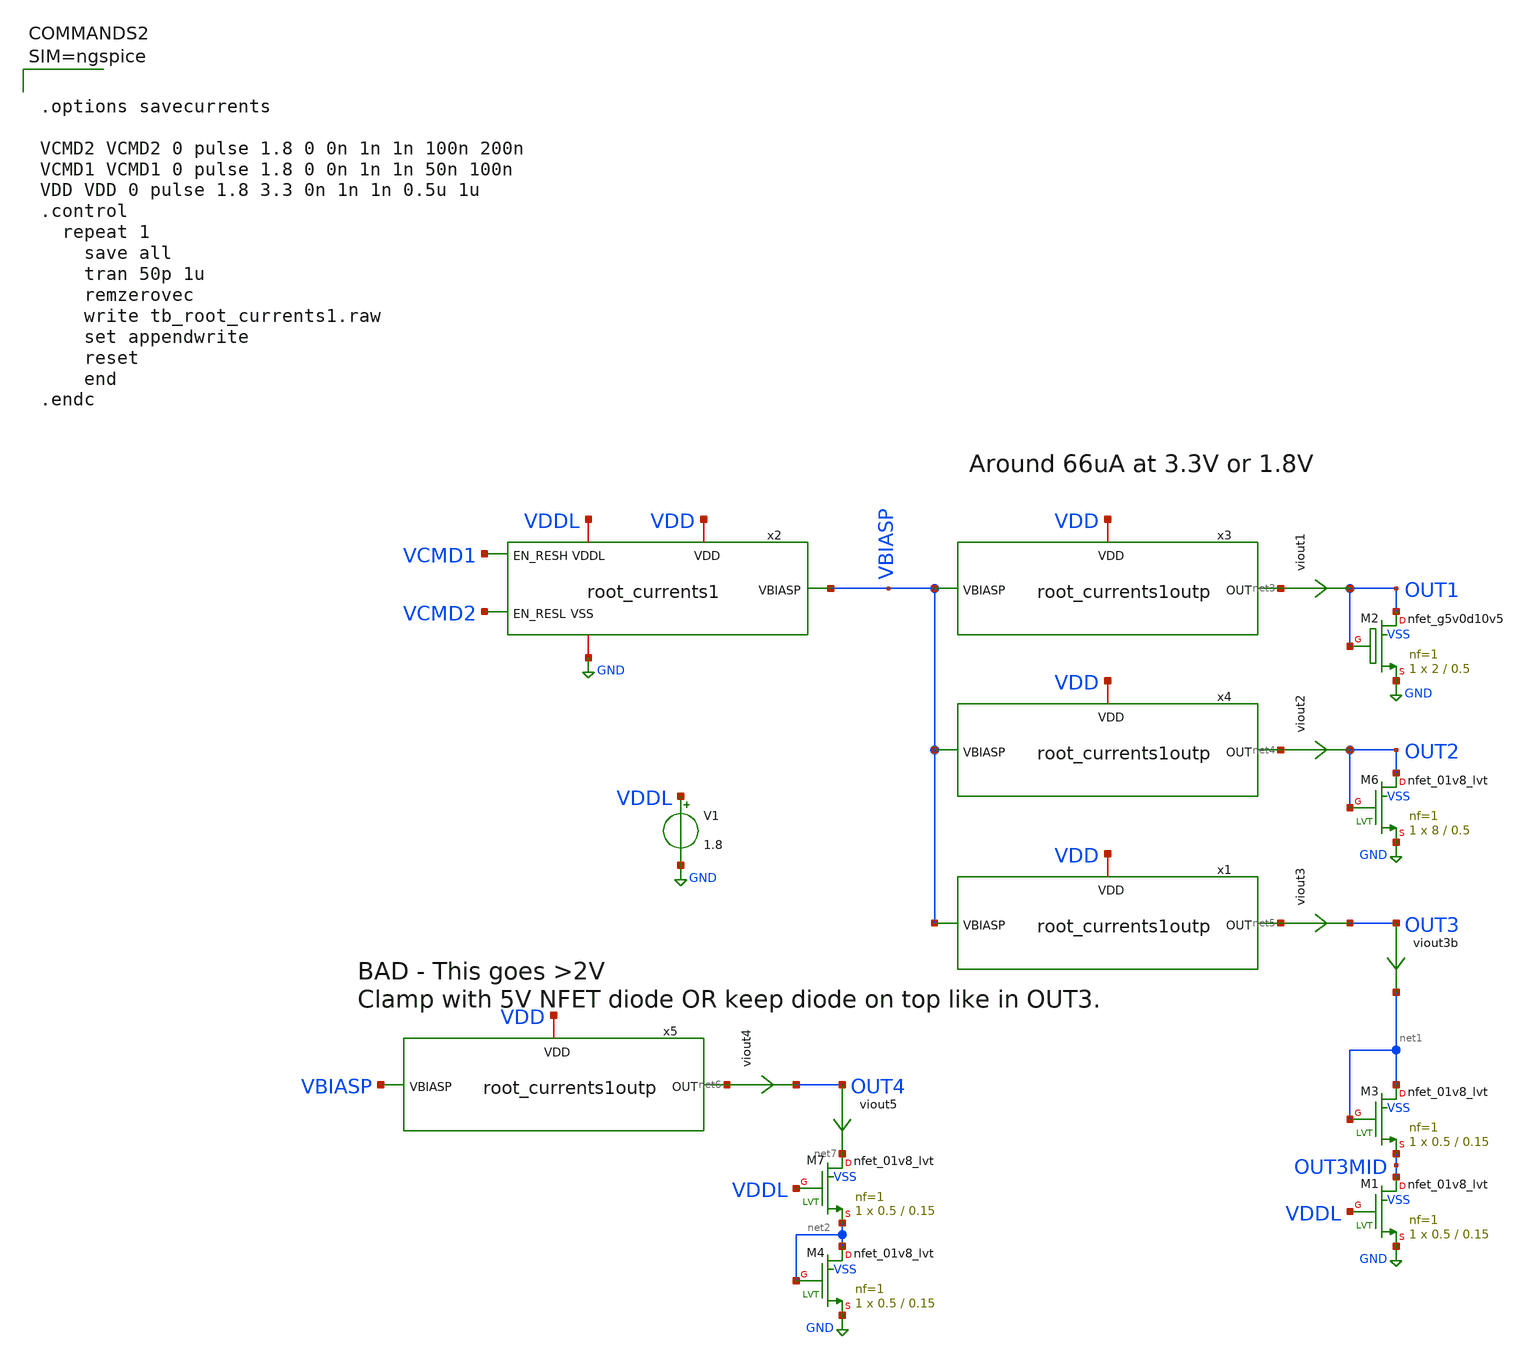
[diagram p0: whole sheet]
** sch_path: xschem/tb_root_currents1.sch
**.subckt tb_root_currents1
x2 VCMD1 VCMD2 VBIASP VDD VDDL GND root_currents1
x3 VBIASP net3 VDD root_currents1outp
x4 VBIASP net4 VDD root_currents1outp
XM6 OUT2 OUT2 GND VSS sky130_fd_pr__nfet_01v8_lvt L=0.5 W=8 nf=1 ad='int((nf+1)/2) * W/nf * 0.29' as='int((nf+2)/2) * W/nf * 0.29'
+ pd='2*int((nf+1)/2) * (W/nf + 0.29)' ps='2*int((nf+2)/2) * (W/nf + 0.29)' nrd='0.29 / W' nrs='0.29 / W'
+ sa=0 sb=0 sd=0 mult=1 m=1
viout1 net3 OUT1 0
.save i(viout1)
viout2 net4 OUT2 0
.save i(viout2)
XM2 OUT1 OUT1 GND VSS sky130_fd_pr__nfet_g5v0d10v5 L=0.5 W=2 nf=1 ad='int((nf+1)/2) * W/nf * 0.29' as='int((nf+2)/2) * W/nf * 0.29'
+ pd='2*int((nf+1)/2) * (W/nf + 0.29)' ps='2*int((nf+2)/2) * (W/nf + 0.29)' nrd='0.29 / W' nrs='0.29 / W'
+ sa=0 sb=0 sd=0 mult=1 m=1
V1 VDDL GND 1.8
x1 VBIASP net5 VDD root_currents1outp
XM1 OUT3MID VDDL GND VSS sky130_fd_pr__nfet_01v8_lvt L=0.15 W=0.5 nf=1 ad='int((nf+1)/2) * W/nf * 0.29'
+ as='int((nf+2)/2) * W/nf * 0.29' pd='2*int((nf+1)/2) * (W/nf + 0.29)' ps='2*int((nf+2)/2) * (W/nf + 0.29)'
+ nrd='0.29 / W' nrs='0.29 / W' sa=0 sb=0 sd=0 mult=1 m=1
viout3 net5 OUT3 0
.save i(viout3)
viout3b OUT3 net1 0
.save i(viout3b)
XM3 net1 net1 OUT3MID VSS sky130_fd_pr__nfet_01v8_lvt L=0.15 W=0.5 nf=1 ad='int((nf+1)/2) * W/nf * 0.29'
+ as='int((nf+2)/2) * W/nf * 0.29' pd='2*int((nf+1)/2) * (W/nf + 0.29)' ps='2*int((nf+2)/2) * (W/nf + 0.29)'
+ nrd='0.29 / W' nrs='0.29 / W' sa=0 sb=0 sd=0 mult=1 m=1
x5 VBIASP net6 VDD root_currents1outp
viout4 net6 OUT4 0
.save i(viout4)
viout5 OUT4 net7 0
.save i(viout5)
XM4 net2 net2 GND VSS sky130_fd_pr__nfet_01v8_lvt L=0.15 W=0.5 nf=1 ad='int((nf+1)/2) * W/nf * 0.29'
+ as='int((nf+2)/2) * W/nf * 0.29' pd='2*int((nf+1)/2) * (W/nf + 0.29)' ps='2*int((nf+2)/2) * (W/nf + 0.29)'
+ nrd='0.29 / W' nrs='0.29 / W' sa=0 sb=0 sd=0 mult=1 m=1
XM7 net7 VDDL net2 VSS sky130_fd_pr__nfet_01v8_lvt L=0.15 W=0.5 nf=1 ad='int((nf+1)/2) * W/nf * 0.29'
+ as='int((nf+2)/2) * W/nf * 0.29' pd='2*int((nf+1)/2) * (W/nf + 0.29)' ps='2*int((nf+2)/2) * (W/nf + 0.29)'
+ nrd='0.29 / W' nrs='0.29 / W' sa=0 sb=0 sd=0 mult=1 m=1
**** begin user architecture code

** opencircuitdesign pdks install
.lib $::SKYWATER_MODELS/sky130.lib.spice tt





.options savecurrents

VCMD2 VCMD2 0 pulse 1.8 0 0n 1n 1n 100n 200n
VCMD1 VCMD1 0 pulse 1.8 0 0n 1n 1n 50n 100n
VDD VDD 0 pulse 1.8 3.3 0n 1n 1n 0.5u 1u
.control
  repeat 1
    save all
    tran 50p 1u
    remzerovec
    write tb_root_currents1.raw
    set appendwrite
    reset
    end
.endc



**** end user architecture code
**.ends

* expanding   symbol:  root_currents1.sym # of pins=6
** sym_path: xschem/root_currents1.sym
** sch_path: xschem/root_currents1.sch
.subckt root_currents1 EN_RESH EN_RESL VBIASP VDD VDDL VSS
*.iopin VSS
*.ipin EN_RESH
*.opin VBIASP
*.iopin VDDL
*.iopin VDD
*.ipin EN_RESL
XR1 V1 net2 net4 sky130_fd_pr__res_high_po_0p35 L=20 mult=1 m=1
XR2 V2 net3 net5 sky130_fd_pr__res_high_po_0p69 L=8 mult=1 m=1
XM4 VMID VMID VSS VSS sky130_fd_pr__nfet_01v8_lvt L=0.5 W=4 nf=1 ad='int((nf+1)/2) * W/nf * 0.29' as='int((nf+2)/2) * W/nf * 0.29'
+ pd='2*int((nf+1)/2) * (W/nf + 0.29)' ps='2*int((nf+2)/2) * (W/nf + 0.29)' nrd='0.29 / W' nrs='0.29 / W'
+ sa=0 sb=0 sd=0 mult=1 m=1
XM5 VMID VMID VSS VSS sky130_fd_pr__nfet_01v8_lvt L=0.5 W=4 nf=1 ad='int((nf+1)/2) * W/nf * 0.29' as='int((nf+2)/2) * W/nf * 0.29'
+ pd='2*int((nf+1)/2) * (W/nf + 0.29)' ps='2*int((nf+2)/2) * (W/nf + 0.29)' nrd='0.29 / W' nrs='0.29 / W'
+ sa=0 sb=0 sd=0 mult=1 m=1
XM6 net1 VMID VSS VSS sky130_fd_pr__nfet_01v8_lvt L=0.5 W=4 nf=1 ad='int((nf+1)/2) * W/nf * 0.29' as='int((nf+2)/2) * W/nf * 0.29'
+ pd='2*int((nf+1)/2) * (W/nf + 0.29)' ps='2*int((nf+2)/2) * (W/nf + 0.29)' nrd='0.29 / W' nrs='0.29 / W'
+ sa=0 sb=0 sd=0 mult=1 m=1
XM2 V1 EN_RESH_VDD VMID VSS sky130_fd_pr__nfet_g5v0d10v5 L=0.5 W=4 nf=1 ad='int((nf+1)/2) * W/nf * 0.29'
+ as='int((nf+2)/2) * W/nf * 0.29' pd='2*int((nf+1)/2) * (W/nf + 0.29)' ps='2*int((nf+2)/2) * (W/nf + 0.29)'
+ nrd='0.29 / W' nrs='0.29 / W' sa=0 sb=0 sd=0 mult=1 m=1
viout VBIASP net1 0
.save i(viout)
x1 EN_RESH EN_RESH_VDD net6 VDD VDDL VSS lvl_shift_lohi1
XM7 VBIASP VBIASP VDD VDD sky130_fd_pr__pfet_g5v0d10v5 L=0.5 W=4 nf=1 ad='int((nf+1)/2) * W/nf * 0.29'
+ as='int((nf+2)/2) * W/nf * 0.29' pd='2*int((nf+1)/2) * (W/nf + 0.29)' ps='2*int((nf+2)/2) * (W/nf + 0.29)'
+ nrd='0.29 / W' nrs='0.29 / W' sa=0 sb=0 sd=0 mult=1 m=1
vin1 VDD net2 0
.save i(vin1)
vin2 VDDL net3 0
.save i(vin2)
XM1 V2 EN_RESL VMID VSS sky130_fd_pr__nfet_01v8_lvt L=0.5 W=4 nf=1 ad='int((nf+1)/2) * W/nf * 0.29' as='int((nf+2)/2) * W/nf * 0.29'
+ pd='2*int((nf+1)/2) * (W/nf + 0.29)' ps='2*int((nf+2)/2) * (W/nf + 0.29)' nrd='0.29 / W' nrs='0.29 / W'
+ sa=0 sb=0 sd=0 mult=1 m=1
.ends


* expanding   symbol:  root_currents1outp.sym # of pins=3
** sym_path: xschem/root_currents1outp.sym
** sch_path: xschem/root_currents1outp.sch
.subckt root_currents1outp VBIASP OUT VDD
*.iopin VBIASP
*.iopin VDD
*.iopin OUT
viout net1 OUT 0
.save i(viout)
XM7 net1 VBIASP VDD VDD sky130_fd_pr__pfet_g5v0d10v5 L=0.5 W=4 nf=1 ad='int((nf+1)/2) * W/nf * 0.29'
+ as='int((nf+2)/2) * W/nf * 0.29' pd='2*int((nf+1)/2) * (W/nf + 0.29)' ps='2*int((nf+2)/2) * (W/nf + 0.29)'
+ nrd='0.29 / W' nrs='0.29 / W' sa=0 sb=0 sd=0 mult=1 m=1
.ends


* expanding   symbol:  lvl_shift_lohi1.sym # of pins=6
** sym_path: xschem/lvl_shift_lohi1.sym
** sch_path: xschem/lvl_shift_lohi1.sch
.subckt lvl_shift_lohi1 D Q QB VDDH VDDL VSS
*.ipin D
*.opin Q
*.opin QB
*.iopin VDDH
*.iopin VDDL
*.iopin VSS
vpwr VDDL net1 0
.save i(vpwr)
XM1 QB Q VDDH VDDH sky130_fd_pr__pfet_g5v0d10v5 L=0.5 W=2 nf=1 ad='int((nf+1)/2) * W/nf * 0.29' as='int((nf+2)/2) * W/nf * 0.29'
+ pd='2*int((nf+1)/2) * (W/nf + 0.29)' ps='2*int((nf+2)/2) * (W/nf + 0.29)' nrd='0.29 / W' nrs='0.29 / W'
+ sa=0 sb=0 sd=0 mult=1 m=1
XM2 Q QB VDDH VDDH sky130_fd_pr__pfet_g5v0d10v5 L=0.5 W=2 nf=1 ad='int((nf+1)/2) * W/nf * 0.29' as='int((nf+2)/2) * W/nf * 0.29'
+ pd='2*int((nf+1)/2) * (W/nf + 0.29)' ps='2*int((nf+2)/2) * (W/nf + 0.29)' nrd='0.29 / W' nrs='0.29 / W'
+ sa=0 sb=0 sd=0 mult=1 m=1
XM3 QB D VSS VSS sky130_fd_pr__nfet_g5v0d10v5 L=0.5 W=4 nf=1 ad='int((nf+1)/2) * W/nf * 0.29' as='int((nf+2)/2) * W/nf * 0.29'
+ pd='2*int((nf+1)/2) * (W/nf + 0.29)' ps='2*int((nf+2)/2) * (W/nf + 0.29)' nrd='0.29 / W' nrs='0.29 / W'
+ sa=0 sb=0 sd=0 mult=1 m=1
XM4 Q DB VSS VSS sky130_fd_pr__nfet_g5v0d10v5 L=0.5 W=4 nf=1 ad='int((nf+1)/2) * W/nf * 0.29' as='int((nf+2)/2) * W/nf * 0.29'
+ pd='2*int((nf+1)/2) * (W/nf + 0.29)' ps='2*int((nf+2)/2) * (W/nf + 0.29)' nrd='0.29 / W' nrs='0.29 / W'
+ sa=0 sb=0 sd=0 mult=1 m=1
XM5 DB D VSS VSS sky130_fd_pr__nfet_01v8_lvt L=0.5 W=1 nf=1 ad='int((nf+1)/2) * W/nf * 0.29' as='int((nf+2)/2) * W/nf * 0.29'
+ pd='2*int((nf+1)/2) * (W/nf + 0.29)' ps='2*int((nf+2)/2) * (W/nf + 0.29)' nrd='0.29 / W' nrs='0.29 / W'
+ sa=0 sb=0 sd=0 mult=1 m=1
XM6 DB D net1 VDDL sky130_fd_pr__pfet_01v8_lvt L=0.5 W=2 nf=1 ad='int((nf+1)/2) * W/nf * 0.29' as='int((nf+2)/2) * W/nf * 0.29'
+ pd='2*int((nf+1)/2) * (W/nf + 0.29)' ps='2*int((nf+2)/2) * (W/nf + 0.29)' nrd='0.29 / W' nrs='0.29 / W'
+ sa=0 sb=0 sd=0 mult=1 m=1
.ends

.GLOBAL GND
.end
